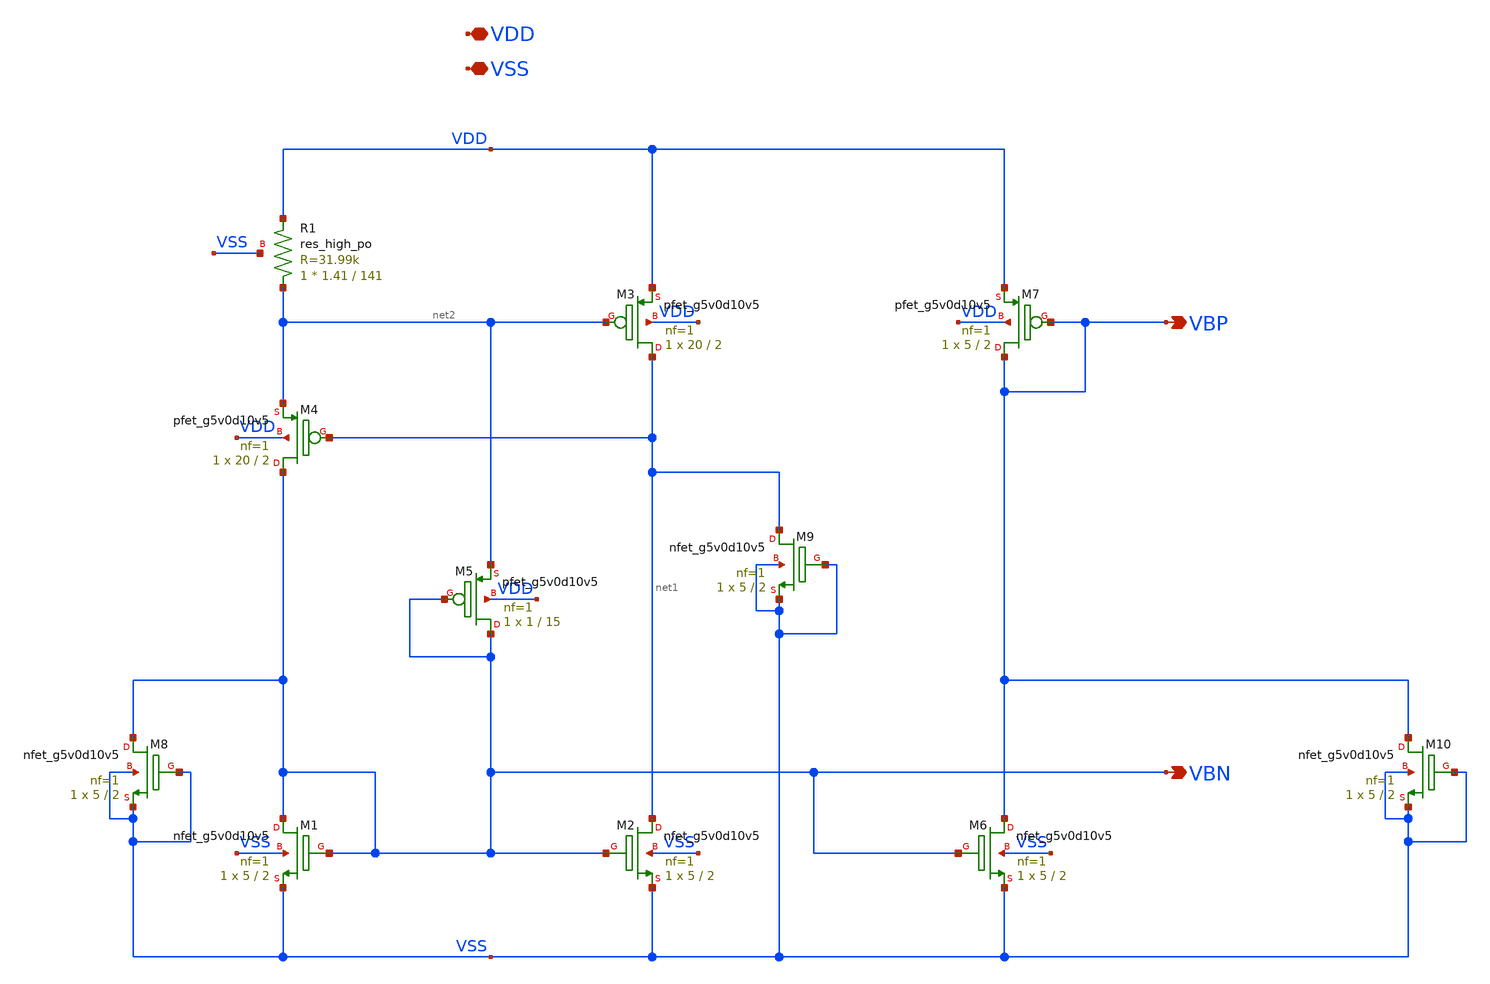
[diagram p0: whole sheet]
** sch_path: spice/xschem/comparator_bias.sch
**.subckt comparator_bias VBP VBN VDD VSS
*.opin VBP
*.opin VBN
*.iopin VDD
*.iopin VSS
XR1 net2 VDD VSS sky130_fd_pr__res_high_po W=1.41 L=141 mult=1 m=1
XM3 net1 net2 VDD VDD sky130_fd_pr__pfet_g5v0d10v5 L=2 W=20 nf=1 ad='int((nf+1)/2) * W/nf * 0.29' as='int((nf+2)/2) * W/nf * 0.29'
+ pd='2*int((nf+1)/2) * (W/nf + 0.29)' ps='2*int((nf+2)/2) * (W/nf + 0.29)' nrd='0.29 / W' nrs='0.29 / W'
+ sa=0 sb=0 sd=0 mult=1 m=1
XM4 VBN net1 net2 VDD sky130_fd_pr__pfet_g5v0d10v5 L=2 W=20 nf=1 ad='int((nf+1)/2) * W/nf * 0.29' as='int((nf+2)/2) * W/nf * 0.29'
+ pd='2*int((nf+1)/2) * (W/nf + 0.29)' ps='2*int((nf+2)/2) * (W/nf + 0.29)' nrd='0.29 / W' nrs='0.29 / W'
+ sa=0 sb=0 sd=0 mult=1 m=1
XM5 VBN VBN net2 VDD sky130_fd_pr__pfet_g5v0d10v5 L=15 W=1 nf=1 ad='int((nf+1)/2) * W/nf * 0.29' as='int((nf+2)/2) * W/nf * 0.29'
+ pd='2*int((nf+1)/2) * (W/nf + 0.29)' ps='2*int((nf+2)/2) * (W/nf + 0.29)' nrd='0.29 / W' nrs='0.29 / W'
+ sa=0 sb=0 sd=0 mult=1 m=1
XM7 VBP VBP VDD VDD sky130_fd_pr__pfet_g5v0d10v5 L=2 W=5 nf=1 ad='int((nf+1)/2) * W/nf * 0.29' as='int((nf+2)/2) * W/nf * 0.29'
+ pd='2*int((nf+1)/2) * (W/nf + 0.29)' ps='2*int((nf+2)/2) * (W/nf + 0.29)' nrd='0.29 / W' nrs='0.29 / W'
+ sa=0 sb=0 sd=0 mult=1 m=1
XM1 VBN VBN VSS VSS sky130_fd_pr__nfet_g5v0d10v5 L=2 W=5 nf=1 ad='int((nf+1)/2) * W/nf * 0.29' as='int((nf+2)/2) * W/nf * 0.29'
+ pd='2*int((nf+1)/2) * (W/nf + 0.29)' ps='2*int((nf+2)/2) * (W/nf + 0.29)' nrd='0.29 / W' nrs='0.29 / W'
+ sa=0 sb=0 sd=0 mult=1 m=1
XM2 net1 VBN VSS VSS sky130_fd_pr__nfet_g5v0d10v5 L=2 W=5 nf=1 ad='int((nf+1)/2) * W/nf * 0.29' as='int((nf+2)/2) * W/nf * 0.29'
+ pd='2*int((nf+1)/2) * (W/nf + 0.29)' ps='2*int((nf+2)/2) * (W/nf + 0.29)' nrd='0.29 / W' nrs='0.29 / W'
+ sa=0 sb=0 sd=0 mult=1 m=1
XM6 VBP VBN VSS VSS sky130_fd_pr__nfet_g5v0d10v5 L=2 W=5 nf=1 ad='int((nf+1)/2) * W/nf * 0.29' as='int((nf+2)/2) * W/nf * 0.29'
+ pd='2*int((nf+1)/2) * (W/nf + 0.29)' ps='2*int((nf+2)/2) * (W/nf + 0.29)' nrd='0.29 / W' nrs='0.29 / W'
+ sa=0 sb=0 sd=0 mult=1 m=1
XM8 VBN VSS VSS VSS sky130_fd_pr__nfet_g5v0d10v5 L=2 W=5 nf=1 ad='int((nf+1)/2) * W/nf * 0.29' as='int((nf+2)/2) * W/nf * 0.29'
+ pd='2*int((nf+1)/2) * (W/nf + 0.29)' ps='2*int((nf+2)/2) * (W/nf + 0.29)' nrd='0.29 / W' nrs='0.29 / W'
+ sa=0 sb=0 sd=0 mult=1 m=1
XM9 net1 VSS VSS VSS sky130_fd_pr__nfet_g5v0d10v5 L=2 W=5 nf=1 ad='int((nf+1)/2) * W/nf * 0.29' as='int((nf+2)/2) * W/nf * 0.29'
+ pd='2*int((nf+1)/2) * (W/nf + 0.29)' ps='2*int((nf+2)/2) * (W/nf + 0.29)' nrd='0.29 / W' nrs='0.29 / W'
+ sa=0 sb=0 sd=0 mult=1 m=1
XM10 VBP VSS VSS VSS sky130_fd_pr__nfet_g5v0d10v5 L=2 W=5 nf=1 ad='int((nf+1)/2) * W/nf * 0.29' as='int((nf+2)/2) * W/nf * 0.29'
+ pd='2*int((nf+1)/2) * (W/nf + 0.29)' ps='2*int((nf+2)/2) * (W/nf + 0.29)' nrd='0.29 / W' nrs='0.29 / W'
+ sa=0 sb=0 sd=0 mult=1 m=1
**.ends
.end
